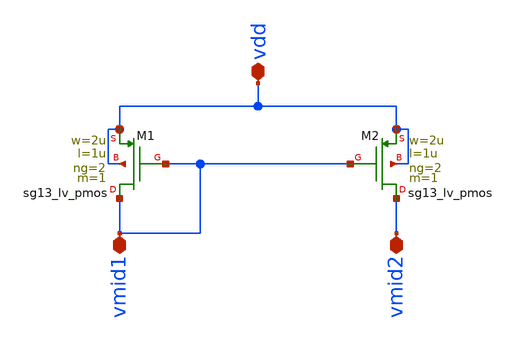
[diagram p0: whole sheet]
** sch_path: AC3E-IHP_ALDO/design_data/klayout/lvs/pmos_cmirror/pmos_current_mirror.sch
**.subckt pmos_current_mirror vdd vmid1 vmid2
*.iopin vdd
*.iopin vmid1
*.iopin vmid2
XM1 vmid1 vmid1 vdd vdd sg13_lv_pmos w=2u l=1u ng=2 m=1 mm_ok=1
XM2 vmid2 vmid1 vdd vdd sg13_lv_pmos w=2u l=1u ng=2 m=1 mm_ok=1
**.ends
.end
